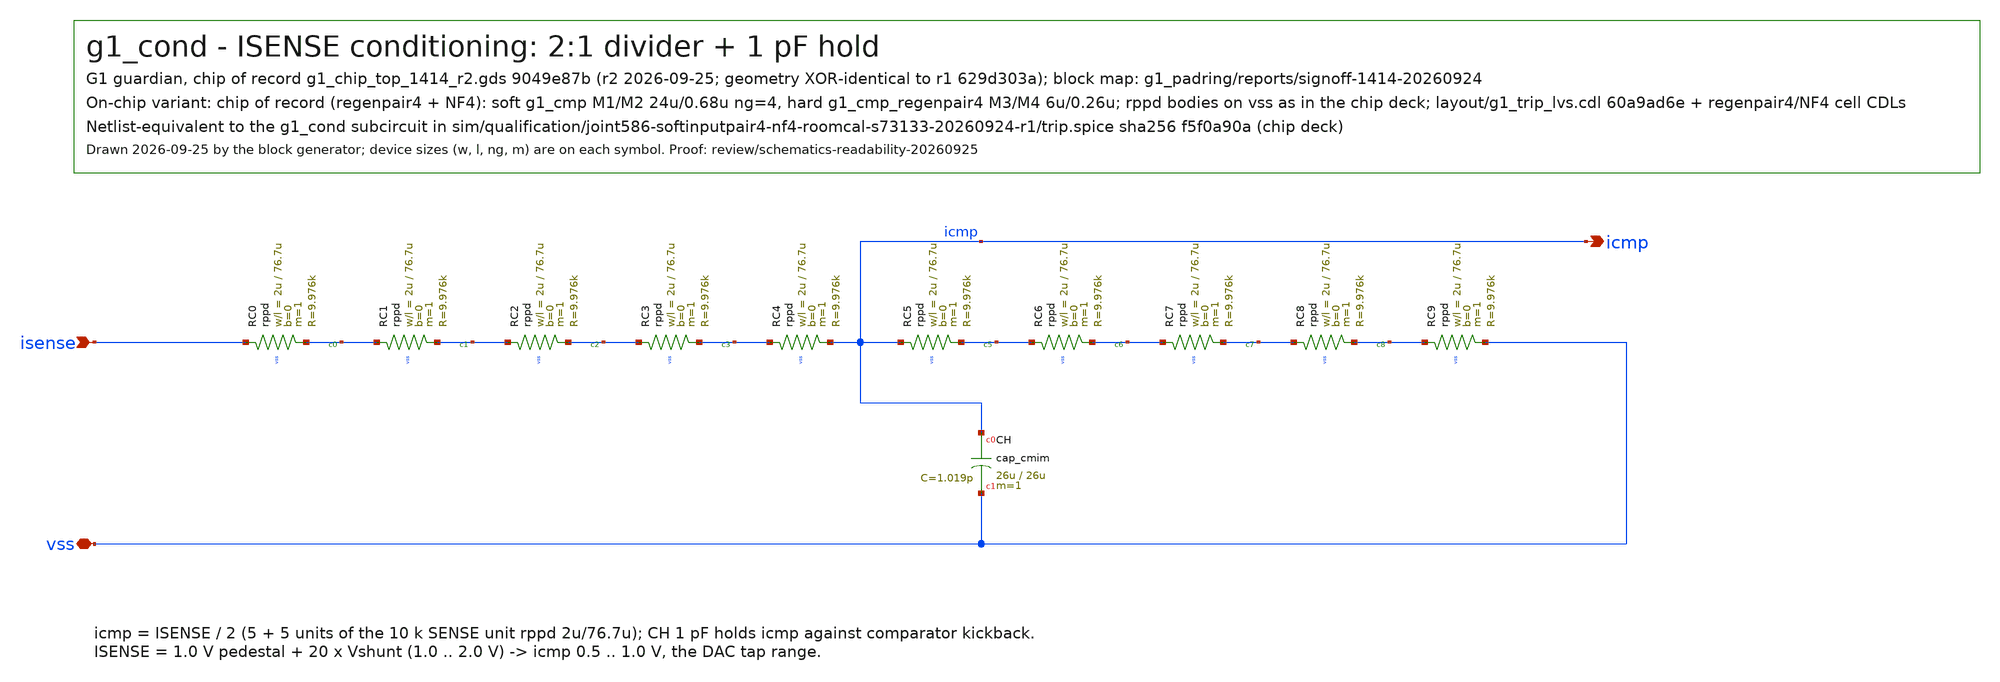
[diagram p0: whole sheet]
** sch_path: designs/g1-guardian/blocks/g1_trip/schematic/g1_cond.sch
**.subckt g1_cond isense icmp vss
*.ipin isense
*.opin icmp
*.iopin vss
XRC0 isense c0 vss rppd w=2u l=76.7u m=1 b=0 mm_ok=1
XRC1 c0 c1 vss rppd w=2u l=76.7u m=1 b=0 mm_ok=1
XRC2 c1 c2 vss rppd w=2u l=76.7u m=1 b=0 mm_ok=1
XRC3 c2 c3 vss rppd w=2u l=76.7u m=1 b=0 mm_ok=1
XRC4 c3 icmp vss rppd w=2u l=76.7u m=1 b=0 mm_ok=1
XRC5 icmp c5 vss rppd w=2u l=76.7u m=1 b=0 mm_ok=1
XRC6 c5 c6 vss rppd w=2u l=76.7u m=1 b=0 mm_ok=1
XRC7 c6 c7 vss rppd w=2u l=76.7u m=1 b=0 mm_ok=1
XRC8 c7 c8 vss rppd w=2u l=76.7u m=1 b=0 mm_ok=1
XRC9 c8 vss vss rppd w=2u l=76.7u m=1 b=0 mm_ok=1
XCH icmp vss cap_cmim w=26u l=26u m=1 mm_ok=1
**.ends
.end
